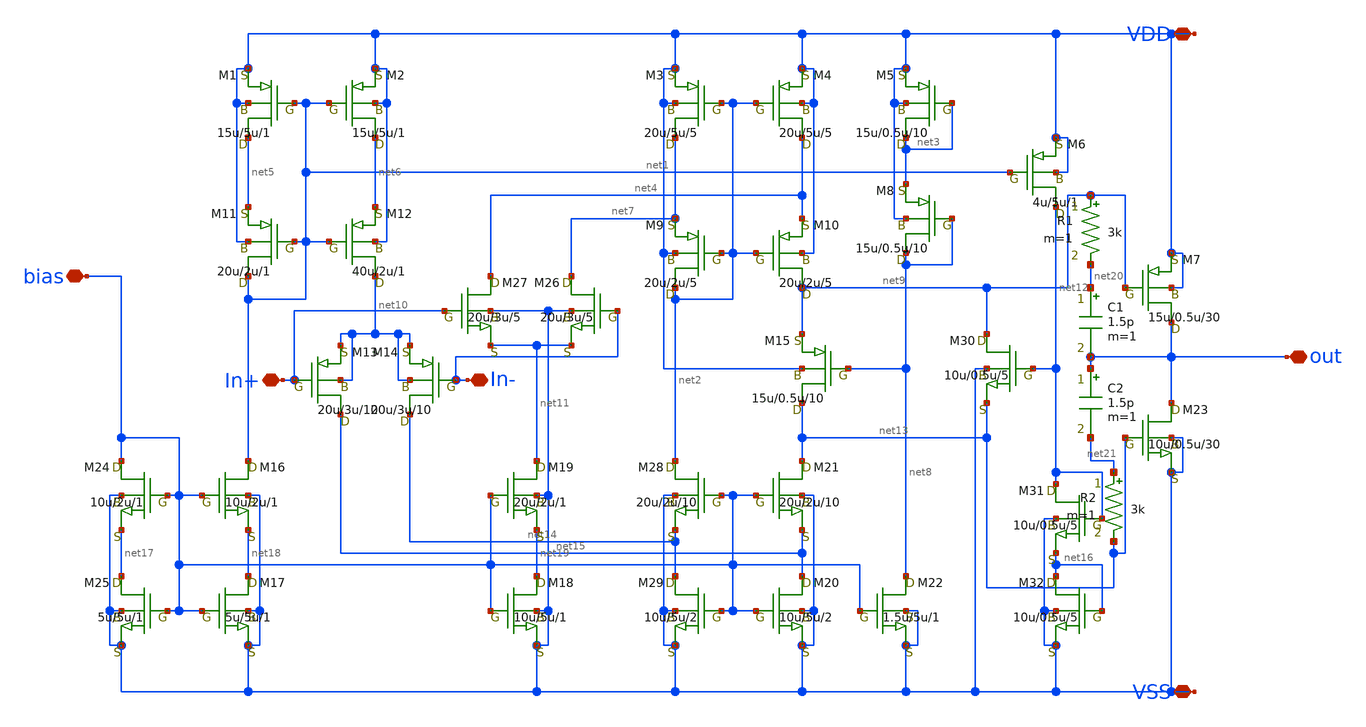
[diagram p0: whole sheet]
** sch_path: Xschem/op8_22_v2.sch
**.subckt op8_22_v2 In+ In- out VDD VSS bias
*.iopin In+
*.iopin In-
*.iopin out
*.iopin VDD
*.iopin VSS
*.iopin bias
C1 net20 out 1.5p m=1
C2 out net21 1.5p m=1
M1 net5 net1 VDD VDD pch w=15u l=5u as=0 ps=0 ad=0 pd=0 m=1
M2 net6 net1 VDD VDD pch w=15u l=5u as=0 ps=0 ad=0 pd=0 m=1
M3 net7 net2 VDD VDD pch w=20u l=5u as=0 ps=0 ad=0 pd=0 m=5
M4 net4 net2 VDD VDD pch w=20u l=5u as=0 ps=0 ad=0 pd=0 m=5
M5 net3 net3 VDD VDD pch w=15u l=0.5u as=0 ps=0 ad=0 pd=0 m=10
M6 net12 net1 VDD VDD pch w=4u l=5u as=0 ps=0 ad=0 pd=0 m=1
M7 out net9 VDD VDD pch w=15u l=0.5u as=0 ps=0 ad=0 pd=0 m=30
M8 net8 net8 net3 VDD pch w=15u l=0.5u as=0 ps=0 ad=0 pd=0 m=10
M9 net2 net2 net7 VDD pch w=20u l=2u as=0 ps=0 ad=0 pd=0 m=5
M10 net9 net2 net4 VDD pch w=20u l=2u as=0 ps=0 ad=0 pd=0 m=5
M11 net1 net1 net5 VDD pch w=20u l=2u as=0 ps=0 ad=0 pd=0 m=1
M12 net10 net1 net6 VDD pch w=40u l=2u as=0 ps=0 ad=0 pd=0 m=1
M13 net15 In+ net10 net10 pch w=20u l=3u as=0 ps=0 ad=0 pd=0 m=10
M14 net14 In- net10 net10 pch w=20u l=3u as=0 ps=0 ad=0 pd=0 m=10
M15 net13 net8 net9 VDD pch w=15u l=0.5u as=0 ps=0 ad=0 pd=0 m=10
M16 net1 bias net18 VSS nch w=10u l=2u as=0 ps=0 ad=0 pd=0 m=1
M17 net18 bias VSS VSS nch w=5u l=5u as=0 ps=0 ad=0 pd=0 m=1
M18 net19 bias VSS VSS nch w=10u l=5u as=0 ps=0 ad=0 pd=0 m=1
M19 net11 bias net19 VSS nch w=20u l=2u as=0 ps=0 ad=0 pd=0 m=1
M21 net13 bias net15 VSS nch w=20u l=2u as=0 ps=0 ad=0 pd=0 m=10
M22 net8 bias VSS VSS nch w=1.5u l=5u as=0 ps=0 ad=0 pd=0 m=1
M23 out net13 VSS VSS nch w=10u l=0.5u as=0 ps=0 ad=0 pd=0 m=30
M24 bias bias net17 VSS nch w=10u l=2u as=0 ps=0 ad=0 pd=0 m=1
M25 net17 bias VSS VSS nch w=5u l=5u as=0 ps=0 ad=0 pd=0 m=1
M26 net7 In- net11 VSS nch w=20u l=3u as=0 ps=0 ad=0 pd=0 m=5
M27 net4 In+ net11 VSS nch w=20u l=3u as=0 ps=0 ad=0 pd=0 m=5
M28 net2 bias net14 VSS nch w=20u l=2u as=0 ps=0 ad=0 pd=0 m=10
M30 net9 net12 net13 VSS nch w=10u l=0.5u as=0 ps=0 ad=0 pd=0 m=5
M31 net12 net12 net16 VSS nch w=10u l=0.5u as=0 ps=0 ad=0 pd=0 m=5
M32 net16 net16 VSS VSS nch w=10u l=0.5u as=0 ps=0 ad=0 pd=0 m=5
M20 net15 bias VSS VSS nch w=10u l=5u as=0 ps=0 ad=0 pd=0 m=2
M29 net14 bias VSS VSS nch w=10u l=5u as=0 ps=0 ad=0 pd=0 m=2
R1 net9 net20 3k m=1
R2 net21 net13 3k m=1
**.ends
.end
